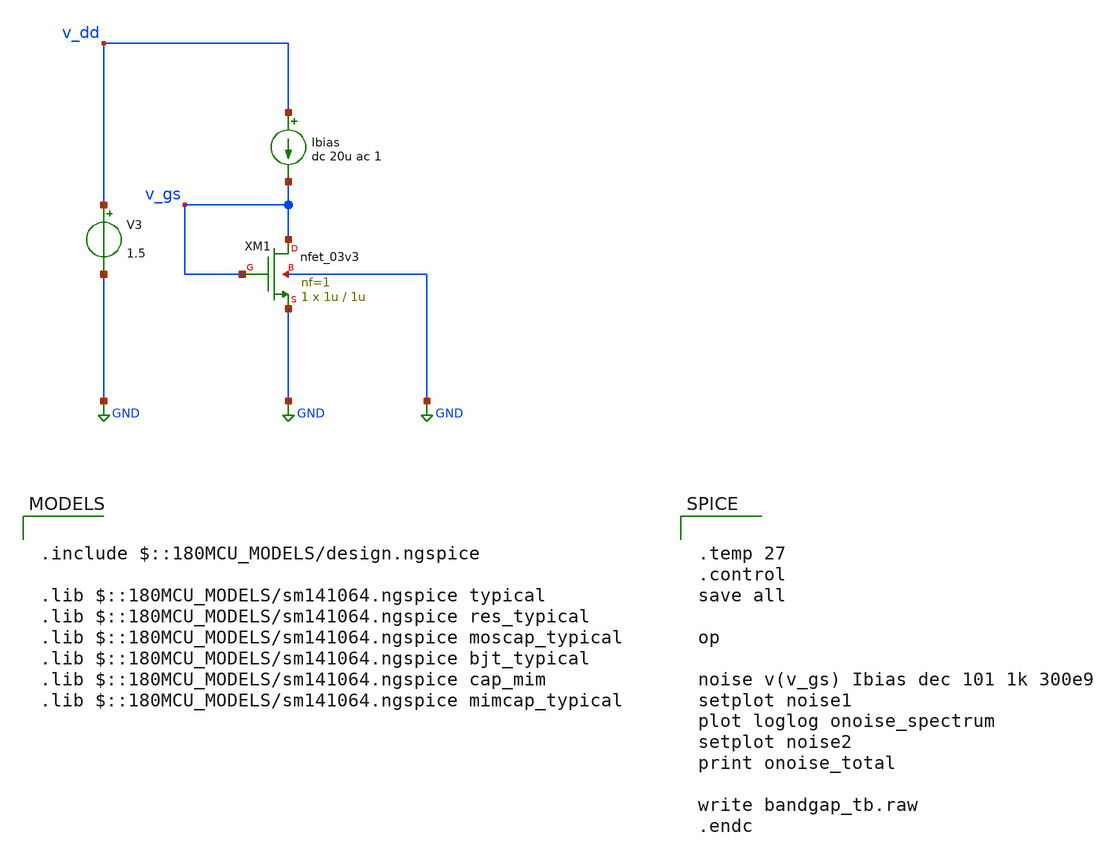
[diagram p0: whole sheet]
** sch_path: bandgap/xschem/sim/noise_test.sch
**.subckt noise_test
Ibias v_dd v_gs dc 20u ac 1
XM1 v_gs v_gs GND GND nfet_03v3 L=1u W=1u nf=1 ad='int((nf+1)/2) * W/nf * 0.18u' as='int((nf+2)/2) * W/nf * 0.18u'
+ pd='2*int((nf+1)/2) * (W/nf + 0.18u)' ps='2*int((nf+2)/2) * (W/nf + 0.18u)' nrd='0.18u / W' nrs='0.18u / W'
+ sa=0 sb=0 sd=0 m=1
V3 v_dd GND 1.5
**** begin user architecture code


.temp 27
.control
save all

op

noise v(v_gs) Ibias dec 101 1k 300e9
setplot noise1
plot loglog onoise_spectrum
setplot noise2
print onoise_total

write bandgap_tb.raw
.endc



.include $::180MCU_MODELS/design.ngspice

.lib $::180MCU_MODELS/sm141064.ngspice typical
.lib $::180MCU_MODELS/sm141064.ngspice res_typical
.lib $::180MCU_MODELS/sm141064.ngspice moscap_typical
.lib $::180MCU_MODELS/sm141064.ngspice bjt_typical
.lib $::180MCU_MODELS/sm141064.ngspice cap_mim
.lib $::180MCU_MODELS/sm141064.ngspice mimcap_typical

**** end user architecture code
**.ends
.GLOBAL GND
.end
